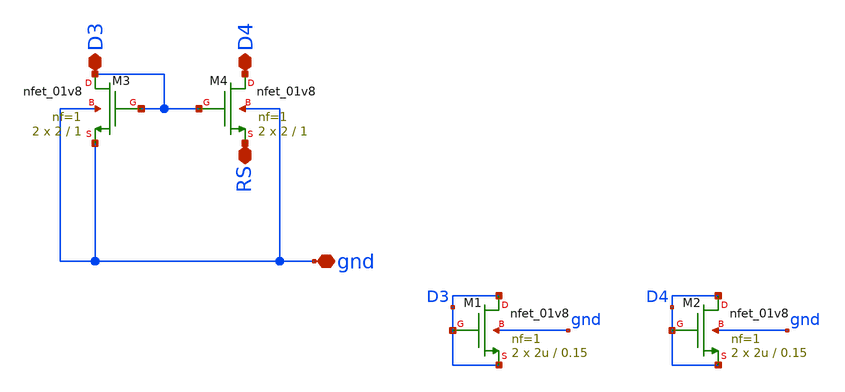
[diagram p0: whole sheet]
** sch_path: opamp/mag/nmos.sch
**.subckt nmos RS gnd D3 D4
*.iopin RS
*.iopin gnd
*.iopin D3
*.iopin D4
XM3 D3 D3 gnd gnd sky130_fd_pr__nfet_01v8 L=1 W=2 nf=1 ad='int((nf+1)/2) * W/nf * 0.29' as='int((nf+2)/2) * W/nf * 0.29'
+ pd='2*int((nf+1)/2) * (W/nf + 0.29)' ps='2*int((nf+2)/2) * (W/nf + 0.29)' nrd='0.29 / W' nrs='0.29 / W'
+ sa=0 sb=0 sd=0 mult=2 m=2
XM4 D4 D3 RS gnd sky130_fd_pr__nfet_01v8 L=1 W=2 nf=1 ad='int((nf+1)/2) * W/nf * 0.29' as='int((nf+2)/2) * W/nf * 0.29'
+ pd='2*int((nf+1)/2) * (W/nf + 0.29)' ps='2*int((nf+2)/2) * (W/nf + 0.29)' nrd='0.29 / W' nrs='0.29 / W'
+ sa=0 sb=0 sd=0 mult=2 m=2
XM1 D3 D3 D3 gnd sky130_fd_pr__nfet_01v8 L=0.15 W=2u nf=1 ad='int((nf+1)/2) * W/nf * 0.29' as='int((nf+2)/2) * W/nf * 0.29'
+ pd='2*int((nf+1)/2) * (W/nf + 0.29)' ps='2*int((nf+2)/2) * (W/nf + 0.29)' nrd='0.29 / W' nrs='0.29 / W'
+ sa=0 sb=0 sd=0 mult=2 m=2
XM2 D4 D4 D4 gnd sky130_fd_pr__nfet_01v8 L=0.15 W=2u nf=1 ad='int((nf+1)/2) * W/nf * 0.29' as='int((nf+2)/2) * W/nf * 0.29'
+ pd='2*int((nf+1)/2) * (W/nf + 0.29)' ps='2*int((nf+2)/2) * (W/nf + 0.29)' nrd='0.29 / W' nrs='0.29 / W'
+ sa=0 sb=0 sd=0 mult=2 m=2
**.ends
.end
